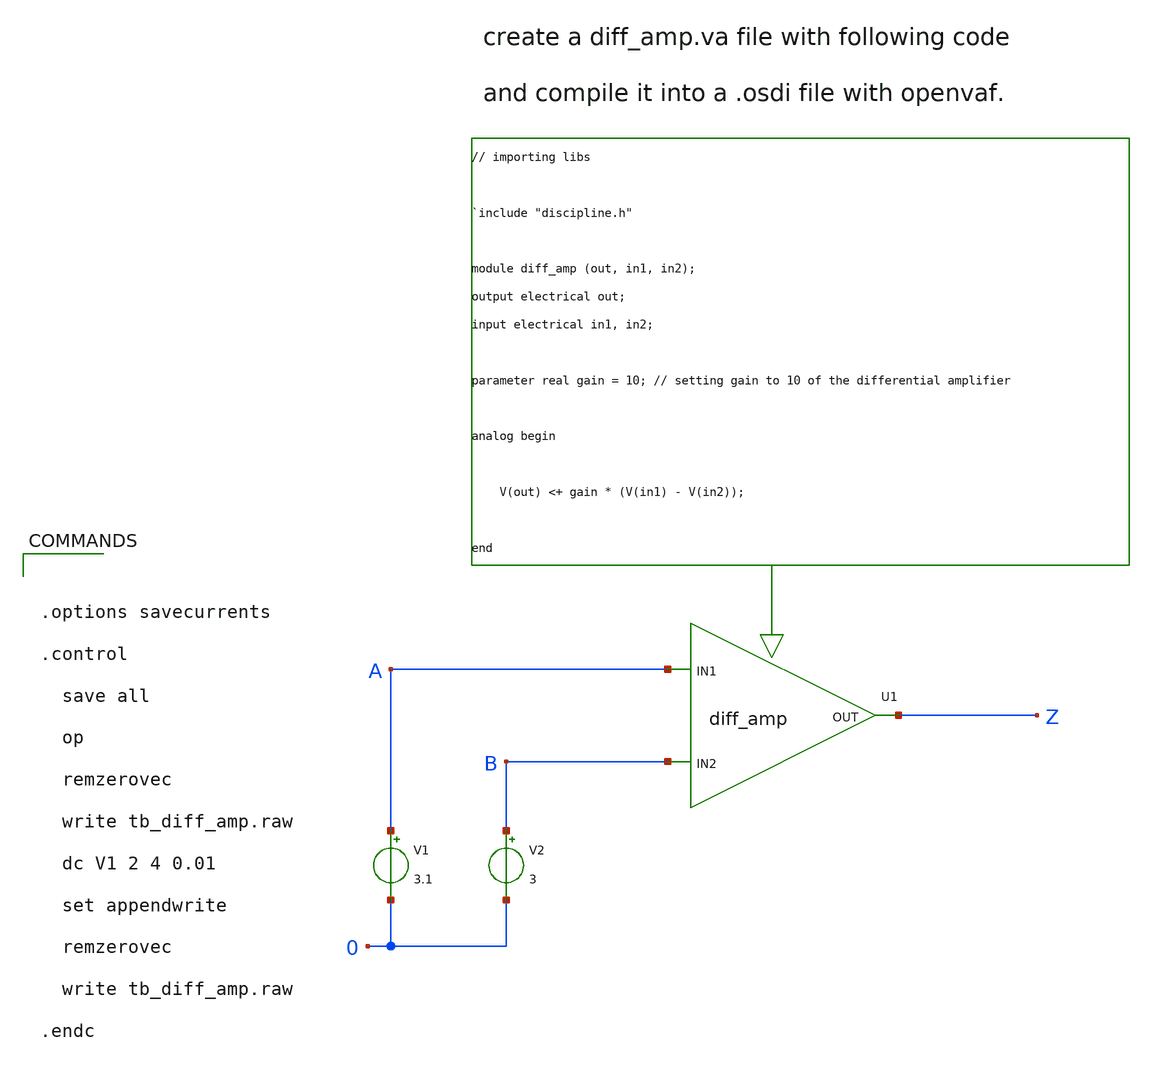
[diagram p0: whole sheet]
** sch_path: schematic/bgr/part_2_full_bgr/schematic/verilog/veriloga_tbs/tb_diff_amp.sch
**.subckt tb_diff_amp
XU1 Z A B diff_amp_cell
V1 A 0 3.1
V2 B 0 3
**** begin user architecture code



.options savecurrents

.control

  save all

  op

  remzerovec

  write tb_diff_amp.raw

  dc V1 2 4 0.01

  set appendwrite

  remzerovec

  write tb_diff_amp.raw

.endc

**** end user architecture code
**.ends
**** begin user architecture code


.subckt diff_amp_cell OUT IN1 IN2

N1 out in1 in2 diff_amp_model

.ends diff_amp_cell



.model diff_amp_model diff_amp



.control

* following line specifies the location for the .osdi file so ngspice can use it.

pre_osdi
+ /home/pedersen/projects/IHP-AnalogAcademy/modules/module_1_bandgap_reference/part_2_full_bgr/schematic/verilog/diff_amp.osdi

.endc


**** end user architecture code
.end
